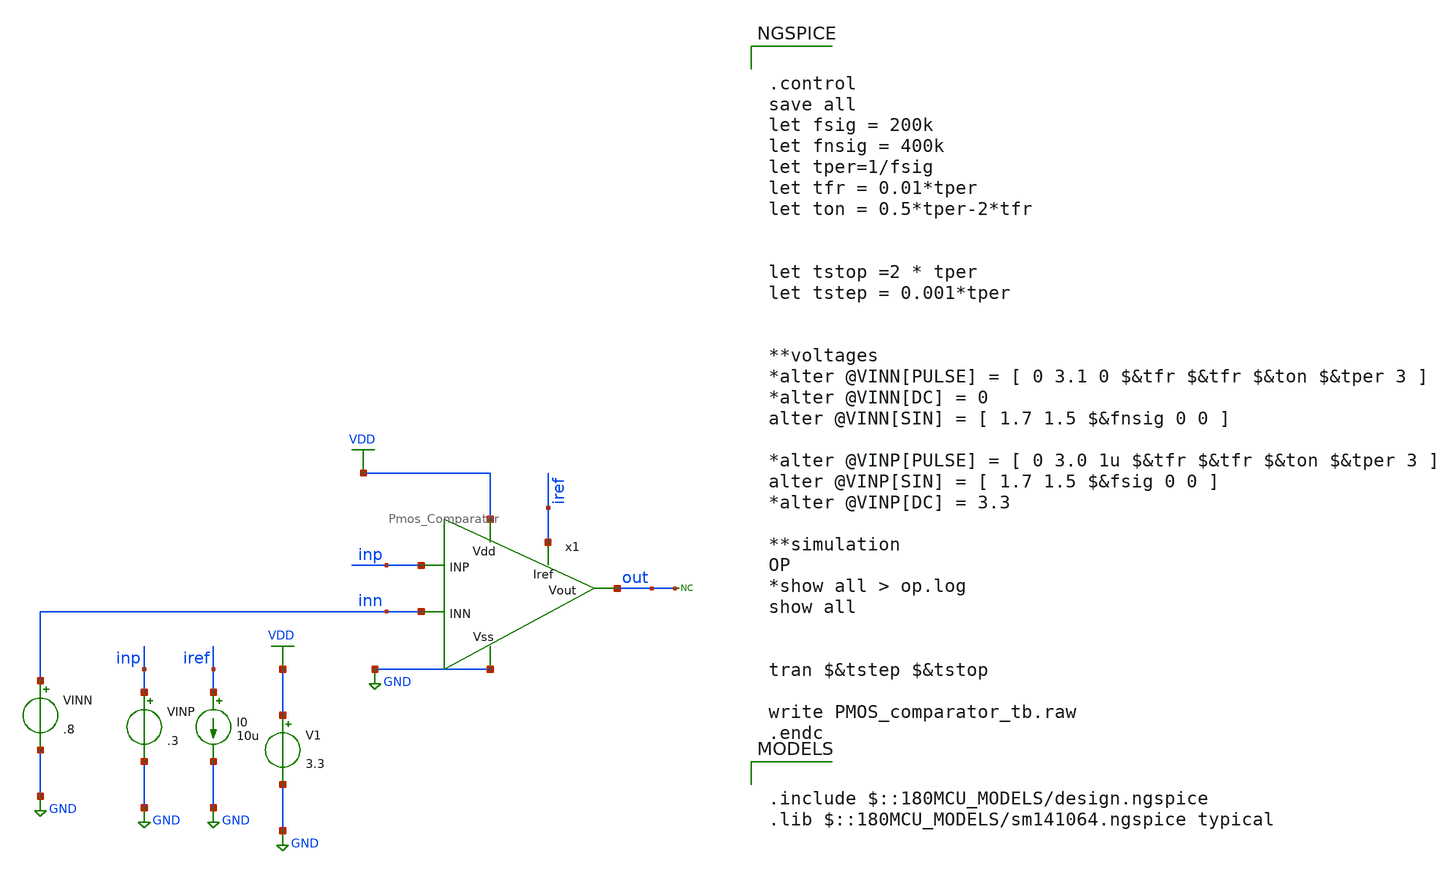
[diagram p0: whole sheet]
** sch_path: designs/libs/tb_analog/tb_Comparator/PMOS_comparator_tb.sch
**.subckt PMOS_comparator_tb
I0 iref GND 10u
V1 VDD GND 3.3
VINP inp GND .3
* noconn out
VINN inn GND .8
x1 VDD iref inp out inn GND Pmos_Comparator
**** begin user architecture code


.control
save all
let fsig = 200k
let fnsig = 400k
let tper=1/fsig
let tfr = 0.01*tper
let ton = 0.5*tper-2*tfr


let tstop =2 * tper
let tstep = 0.001*tper


**voltages
*alter @VINN[PULSE] = [ 0 3.1 0 $&tfr $&tfr $&ton $&tper 3 ]
*alter @VINN[DC] = 0
alter @VINN[SIN] = [ 1.7 1.5 $&fnsig 0 0 ]

*alter @VINP[PULSE] = [ 0 3.0 1u $&tfr $&tfr $&ton $&tper 3 ]
alter @VINP[SIN] = [ 1.7 1.5 $&fsig 0 0 ]
*alter @VINP[DC] = 3.3

**simulation
OP
*show all > op.log
show all


tran $&tstep $&tstop

write PMOS_comparator_tb.raw
.endc



.include $::180MCU_MODELS/design.ngspice
.lib $::180MCU_MODELS/sm141064.ngspice typical

**** end user architecture code
**.ends

* expanding   symbol:  libs/core_analog/Comparator/Pmos_Comparator.sym # of pins=6
** sym_path: designs/libs/core_analog/Comparator/Pmos_Comparator.sym
** sch_path: designs/libs/core_analog/Comparator/Pmos_Comparator.sch
.subckt Pmos_Comparator Vdd Iref INP Vout INN Vss
*.ipin vdd
*.ipin vss
*.ipin iref
*.ipin inn
*.ipin inp
*.opin vout
XM3 net1 net1 vdd vdd pfet_03v3 L=0.6u W=25u nf=5 ad='int((nf+1)/2) * W/nf * 0.18u' as='int((nf+2)/2) * W/nf * 0.18u'
+ pd='2*int((nf+1)/2) * (W/nf + 0.18u)' ps='2*int((nf+2)/2) * (W/nf + 0.18u)' nrd='0.18u / W' nrs='0.18u / W'
+ sa=0 sb=0 sd=0 m=1
XM4 vout net1 vdd vdd pfet_03v3 L=0.6u W=25u nf=5 ad='int((nf+1)/2) * W/nf * 0.18u' as='int((nf+2)/2) * W/nf * 0.18u'
+ pd='2*int((nf+1)/2) * (W/nf + 0.18u)' ps='2*int((nf+2)/2) * (W/nf + 0.18u)' nrd='0.18u / W' nrs='0.18u / W'
+ sa=0 sb=0 sd=0 m=1
XM5 net2 inn net3 vdd pfet_03v3 L=1u W=12u nf=4 ad='int((nf+1)/2) * W/nf * 0.18u' as='int((nf+2)/2) * W/nf * 0.18u'
+ pd='2*int((nf+1)/2) * (W/nf + 0.18u)' ps='2*int((nf+2)/2) * (W/nf + 0.18u)' nrd='0.18u / W' nrs='0.18u / W'
+ sa=0 sb=0 sd=0 m=1
XM6 net4 inp net3 vdd pfet_03v3 L=1u W=12u nf=4 ad='int((nf+1)/2) * W/nf * 0.18u' as='int((nf+2)/2) * W/nf * 0.18u'
+ pd='2*int((nf+1)/2) * (W/nf + 0.18u)' ps='2*int((nf+2)/2) * (W/nf + 0.18u)' nrd='0.18u / W' nrs='0.18u / W'
+ sa=0 sb=0 sd=0 m=1
XM7 net1 net2 vss vss nfet_03v3 L=1u W=5.5u nf=1 ad='int((nf+1)/2) * W/nf * 0.18u' as='int((nf+2)/2) * W/nf * 0.18u'
+ pd='2*int((nf+1)/2) * (W/nf + 0.18u)' ps='2*int((nf+2)/2) * (W/nf + 0.18u)' nrd='0.18u / W' nrs='0.18u / W'
+ sa=0 sb=0 sd=0 m=1
XM8 net2 net4 vss vss nfet_03v3 L=1u W=5.5u nf=1 ad='int((nf+1)/2) * W/nf * 0.18u' as='int((nf+2)/2) * W/nf * 0.18u'
+ pd='2*int((nf+1)/2) * (W/nf + 0.18u)' ps='2*int((nf+2)/2) * (W/nf + 0.18u)' nrd='0.18u / W' nrs='0.18u / W'
+ sa=0 sb=0 sd=0 m=1
XM9 net4 net4 vss vss nfet_03v3 L=1u W=5.5u nf=1 ad='int((nf+1)/2) * W/nf * 0.18u' as='int((nf+2)/2) * W/nf * 0.18u'
+ pd='2*int((nf+1)/2) * (W/nf + 0.18u)' ps='2*int((nf+2)/2) * (W/nf + 0.18u)' nrd='0.18u / W' nrs='0.18u / W'
+ sa=0 sb=0 sd=0 m=1
XM10 net4 net2 vss vss nfet_03v3 L=1u W=5.5u nf=1 ad='int((nf+1)/2) * W/nf * 0.18u' as='int((nf+2)/2) * W/nf * 0.18u'
+ pd='2*int((nf+1)/2) * (W/nf + 0.18u)' ps='2*int((nf+2)/2) * (W/nf + 0.18u)' nrd='0.18u / W' nrs='0.18u / W'
+ sa=0 sb=0 sd=0 m=1
XM11 net2 net2 vss vss nfet_03v3 L=1u W=5.5u nf=1 ad='int((nf+1)/2) * W/nf * 0.18u' as='int((nf+2)/2) * W/nf * 0.18u'
+ pd='2*int((nf+1)/2) * (W/nf + 0.18u)' ps='2*int((nf+2)/2) * (W/nf + 0.18u)' nrd='0.18u / W' nrs='0.18u / W'
+ sa=0 sb=0 sd=0 m=1
XM12 vout net4 vss vss nfet_03v3 L=1u W=5.5u nf=1 ad='int((nf+1)/2) * W/nf * 0.18u' as='int((nf+2)/2) * W/nf * 0.18u'
+ pd='2*int((nf+1)/2) * (W/nf + 0.18u)' ps='2*int((nf+2)/2) * (W/nf + 0.18u)' nrd='0.18u / W' nrs='0.18u / W'
+ sa=0 sb=0 sd=0 m=1
x1 vdd vdd iref iref unit_pmos M=2
x2 vdd vdd iref net3 unit_pmos M=4
.ends


* expanding   symbol:  libs/core_analog/unit_pmos/unit_pmos.sym # of pins=4
** sym_path: libs/core_analog/unit_pmos/unit_pmos.sym
** sch_path: libs/core_analog/unit_pmos/unit_pmos.sch
.subckt unit_pmos drain sub gate source
*.iopin drain
*.iopin source
*.iopin sub
*.iopin gate
**** begin user architecture code

.param M=1

**** end user architecture code
XM3 drain gate source sub pfet_03v3 L=1u W=3.5u nf=1 ad='int((nf+1)/2) * W/nf * 0.18u' as='int((nf+2)/2) * W/nf * 0.18u'
+ pd='2*int((nf+1)/2) * (W/nf + 0.18u)' ps='2*int((nf+2)/2) * (W/nf + 0.18u)' nrd='0.18u / W' nrs='0.18u / W'
+ sa=0 sb=0 sd=0 m={M}
.ends

.GLOBAL GND
.GLOBAL VDD
.end
